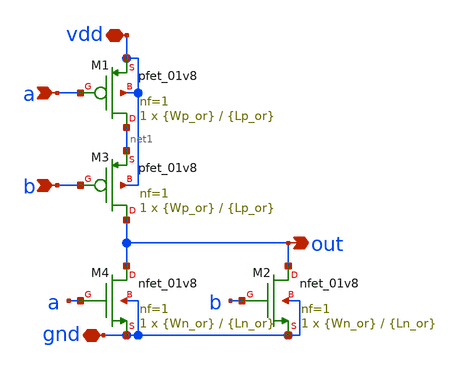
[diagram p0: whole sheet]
** sch_path: inhibitory/nor_2.sch
**.subckt nor_2 gnd a b out vdd
*.iopin gnd
*.ipin a
*.ipin b
*.opin out
*.iopin vdd
XM1 net1 a vdd vdd sky130_fd_pr__pfet_01v8 L={Lp_or} W={Wp_or} nf=1 ad='int((nf+1)/2) * W/nf * 0.29'
+ as='int((nf+2)/2) * W/nf * 0.29' pd='2*int((nf+1)/2) * (W/nf + 0.29)' ps='2*int((nf+2)/2) * (W/nf + 0.29)'
+ nrd='0.29 / W' nrs='0.29 / W' sa=0 sb=0 sd=0 mult=1 m=1
XM2 out b gnd gnd sky130_fd_pr__nfet_01v8 L={Ln_or} W={Wn_or} nf=1 ad='int((nf+1)/2) * W/nf * 0.29' as='int((nf+2)/2) * W/nf * 0.29'
+ pd='2*int((nf+1)/2) * (W/nf + 0.29)' ps='2*int((nf+2)/2) * (W/nf + 0.29)' nrd='0.29 / W' nrs='0.29 / W'
+ sa=0 sb=0 sd=0 mult=1 m=1
XM3 out b net1 vdd sky130_fd_pr__pfet_01v8 L={Lp_or} W={Wp_or} nf=1 ad='int((nf+1)/2) * W/nf * 0.29'
+ as='int((nf+2)/2) * W/nf * 0.29' pd='2*int((nf+1)/2) * (W/nf + 0.29)' ps='2*int((nf+2)/2) * (W/nf + 0.29)'
+ nrd='0.29 / W' nrs='0.29 / W' sa=0 sb=0 sd=0 mult=1 m=1
XM4 out a gnd gnd sky130_fd_pr__nfet_01v8 L={Ln_or} W={Wn_or} nf=1 ad='int((nf+1)/2) * W/nf * 0.29' as='int((nf+2)/2) * W/nf * 0.29'
+ pd='2*int((nf+1)/2) * (W/nf + 0.29)' ps='2*int((nf+2)/2) * (W/nf + 0.29)' nrd='0.29 / W' nrs='0.29 / W'
+ sa=0 sb=0 sd=0 mult=1 m=1
**.ends
.end
